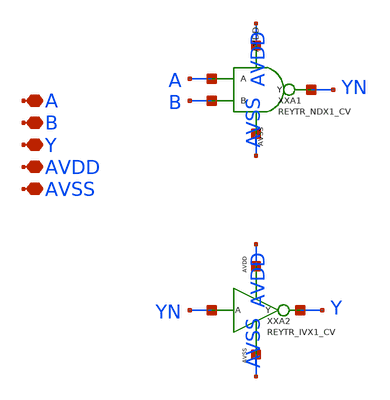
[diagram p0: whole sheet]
** sch_path: design/REY_TR_SKY130A/REYTR_ANX1_CV.sch
**.subckt REYTR_ANX1_CV A B Y AVDD AVSS
*.iopin A
*.iopin B
*.iopin Y
*.iopin AVDD
*.iopin AVSS
XXA1 A B YN AVDD AVSS REYTR_NDX1_CV
XXA2 YN Y AVDD AVSS REYTR_IVX1_CV
**.ends
.end
